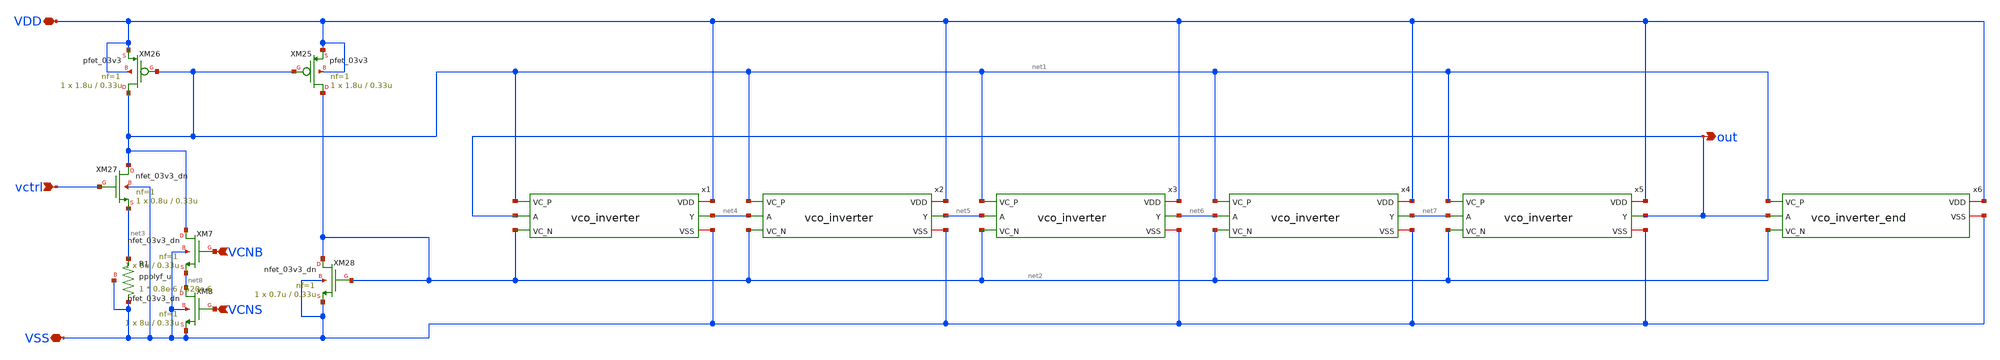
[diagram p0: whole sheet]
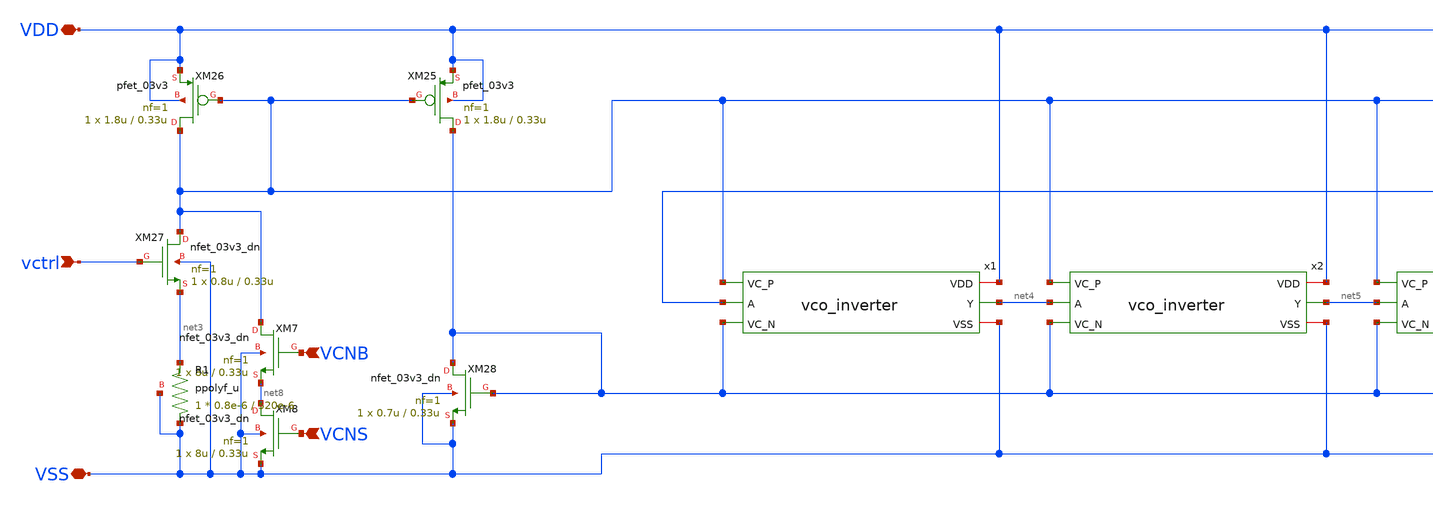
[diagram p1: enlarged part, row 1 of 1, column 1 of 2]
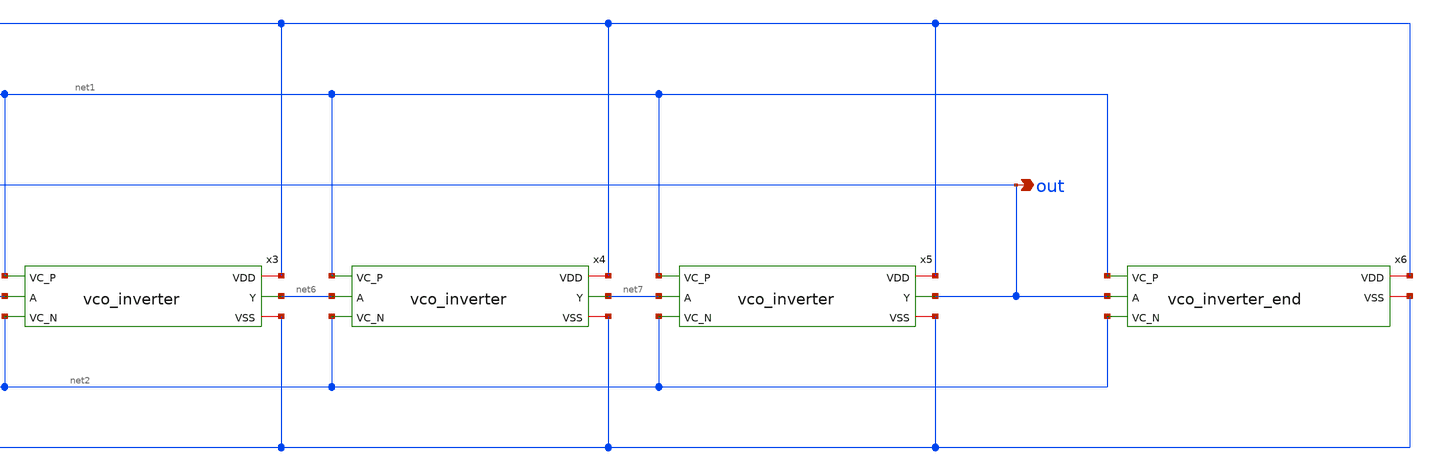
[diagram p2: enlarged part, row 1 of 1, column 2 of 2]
** sch_path: 1st_Design/vco_pex.sch
**.subckt vco_pex out vctrl VCNB VCNS VDD VSS
*.opin out
*.ipin vctrl
*.ipin VCNB
*.ipin VCNS
*.iopin VDD
*.iopin VSS
XM25 net2 net1 VDD VDD pfet_03v3 L=0.33u W=1.8u nf=1 ad='int((nf+1)/2) * W/nf * 0.18u' as='int((nf+2)/2) * W/nf * 0.18u'
+ pd='2*int((nf+1)/2) * (W/nf + 0.18u)' ps='2*int((nf+2)/2) * (W/nf + 0.18u)' nrd='0.18u / W' nrs='0.18u / W'
+ sa=0 sb=0 sd=0 m=1
XM26 net1 net1 VDD VDD pfet_03v3 L=0.33u W=1.8u nf=1 ad='int((nf+1)/2) * W/nf * 0.18u' as='int((nf+2)/2) * W/nf * 0.18u'
+ pd='2*int((nf+1)/2) * (W/nf + 0.18u)' ps='2*int((nf+2)/2) * (W/nf + 0.18u)' nrd='0.18u / W' nrs='0.18u / W'
+ sa=0 sb=0 sd=0 m=1
XM27 net1 vctrl net3 VSS nfet_03v3_dn L=0.33u W=0.8u nf=1 ad='int((nf+1)/2) * W/nf * 0.18u' as='int((nf+2)/2) * W/nf * 0.18u'
+ pd='2*int((nf+1)/2) * (W/nf + 0.18u)' ps='2*int((nf+2)/2) * (W/nf + 0.18u)' nrd='0.18u / W' nrs='0.18u / W'
+ sa=0 sb=0 sd=0 m=1
XM28 net2 net2 VSS VSS nfet_03v3_dn L=0.33u W=0.7u nf=1 ad='int((nf+1)/2) * W/nf * 0.18u' as='int((nf+2)/2) * W/nf * 0.18u'
+ pd='2*int((nf+1)/2) * (W/nf + 0.18u)' ps='2*int((nf+2)/2) * (W/nf + 0.18u)' nrd='0.18u / W' nrs='0.18u / W'
+ sa=0 sb=0 sd=0 m=1
x1 VDD net1 out net4 net2 VSS vco_inverter
x2 VDD net1 net4 net5 net2 VSS vco_inverter
x3 VDD net1 net5 net6 net2 VSS vco_inverter
x4 VDD net1 net6 net7 net2 VSS vco_inverter
x5 VDD net1 net7 out net2 VSS vco_inverter
x6 VDD net1 out net2 VSS vco_inverter_end
XM7 net1 VCNB net8 VSS nfet_03v3_dn L=0.33u W=8u nf=1 ad='int((nf+1)/2) * W/nf * 0.18u' as='int((nf+2)/2) * W/nf * 0.18u'
+ pd='2*int((nf+1)/2) * (W/nf + 0.18u)' ps='2*int((nf+2)/2) * (W/nf + 0.18u)' nrd='0.18u / W' nrs='0.18u / W'
+ sa=0 sb=0 sd=0 m=1
XM8 net8 VCNS VSS VSS nfet_03v3_dn L=0.33u W=8u nf=1 ad='int((nf+1)/2) * W/nf * 0.18u' as='int((nf+2)/2) * W/nf * 0.18u'
+ pd='2*int((nf+1)/2) * (W/nf + 0.18u)' ps='2*int((nf+2)/2) * (W/nf + 0.18u)' nrd='0.18u / W' nrs='0.18u / W'
+ sa=0 sb=0 sd=0 m=1
XR1 VSS net3 VSS ppolyf_u r_width=0.8e-6 r_length=520e-6 m=1
**.ends

* expanding   symbol:  vco_inverter.sym # of pins=6
** sym_path: 1st_Design/vco_inverter.sym
** sch_path: 1st_Design/vco_inverter.sch
.subckt vco_inverter VDD VC_P A Y VC_N VSS
*.iopin VDD
*.iopin VSS
*.ipin A
*.ipin VC_N
*.ipin VC_P
*.opin Y
XM1 net1 VC_P VDD VDD pfet_03v3 L=0.33u W=0.9u nf=1 ad='int((nf+1)/2) * W/nf * 0.18u' as='int((nf+2)/2) * W/nf * 0.18u'
+ pd='2*int((nf+1)/2) * (W/nf + 0.18u)' ps='2*int((nf+2)/2) * (W/nf + 0.18u)' nrd='0.18u / W' nrs='0.18u / W'
+ sa=0 sb=0 sd=0 m=1
XM2 Y A net1 VDD pfet_03v3 L=0.33u W=1.8u nf=1 ad='int((nf+1)/2) * W/nf * 0.18u' as='int((nf+2)/2) * W/nf * 0.18u'
+ pd='2*int((nf+1)/2) * (W/nf + 0.18u)' ps='2*int((nf+2)/2) * (W/nf + 0.18u)' nrd='0.18u / W' nrs='0.18u / W'
+ sa=0 sb=0 sd=0 m=1
XM3 Y A net2 VSS nfet_03v3_dn L=0.33u W=0.84u nf=1 ad='int((nf+1)/2) * W/nf * 0.18u' as='int((nf+2)/2) * W/nf * 0.18u'
+ pd='2*int((nf+1)/2) * (W/nf + 0.18u)' ps='2*int((nf+2)/2) * (W/nf + 0.18u)' nrd='0.18u / W' nrs='0.18u / W'
+ sa=0 sb=0 sd=0 m=1
XM4 net2 VC_N VSS VSS nfet_03v3_dn L=0.33u W=0.42u nf=1 ad='int((nf+1)/2) * W/nf * 0.18u' as='int((nf+2)/2) * W/nf * 0.18u'
+ pd='2*int((nf+1)/2) * (W/nf + 0.18u)' ps='2*int((nf+2)/2) * (W/nf + 0.18u)' nrd='0.18u / W' nrs='0.18u / W'
+ sa=0 sb=0 sd=0 m=1
.ends


* expanding   symbol:  vco_inverter_end.sym # of pins=5
** sym_path: 1st_Design/vco_inverter_end.sym
** sch_path: 1st_Design/vco_inverter_end.sch
.subckt vco_inverter_end VDD VC_P A VC_N VSS
*.iopin VDD
*.iopin VSS
*.ipin A
*.ipin VC_N
*.ipin VC_P
XM1 net1 VC_P VDD VDD pfet_03v3 L=0.33u W=0.9u nf=1 ad='int((nf+1)/2) * W/nf * 0.18u' as='int((nf+2)/2) * W/nf * 0.18u'
+ pd='2*int((nf+1)/2) * (W/nf + 0.18u)' ps='2*int((nf+2)/2) * (W/nf + 0.18u)' nrd='0.18u / W' nrs='0.18u / W'
+ sa=0 sb=0 sd=0 m=1
XM2 net2 A net1 VDD pfet_03v3 L=0.33u W=1.8u nf=1 ad='int((nf+1)/2) * W/nf * 0.18u' as='int((nf+2)/2) * W/nf * 0.18u'
+ pd='2*int((nf+1)/2) * (W/nf + 0.18u)' ps='2*int((nf+2)/2) * (W/nf + 0.18u)' nrd='0.18u / W' nrs='0.18u / W'
+ sa=0 sb=0 sd=0 m=1
XM3 net2 A net3 VSS nfet_03v3_dn L=0.33u W=0.84u nf=1 ad='int((nf+1)/2) * W/nf * 0.18u' as='int((nf+2)/2) * W/nf * 0.18u'
+ pd='2*int((nf+1)/2) * (W/nf + 0.18u)' ps='2*int((nf+2)/2) * (W/nf + 0.18u)' nrd='0.18u / W' nrs='0.18u / W'
+ sa=0 sb=0 sd=0 m=1
XM4 net3 VC_N VSS VSS nfet_03v3_dn L=0.33u W=0.42u nf=1 ad='int((nf+1)/2) * W/nf * 0.18u' as='int((nf+2)/2) * W/nf * 0.18u'
+ pd='2*int((nf+1)/2) * (W/nf + 0.18u)' ps='2*int((nf+2)/2) * (W/nf + 0.18u)' nrd='0.18u / W' nrs='0.18u / W'
+ sa=0 sb=0 sd=0 m=1
.ends

.end
